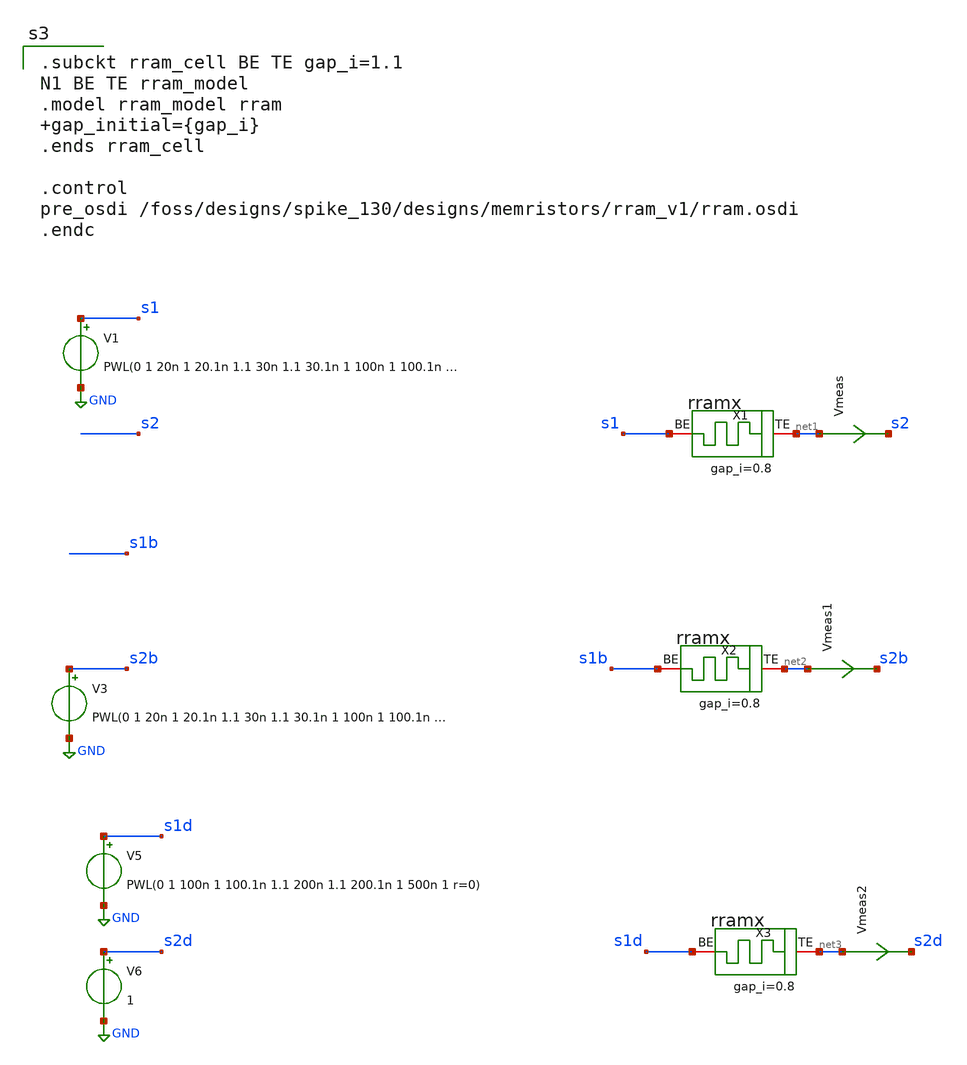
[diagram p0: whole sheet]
** sch_path: designs/tb_memristor/tb_stdp2.sch
**.subckt tb_stdp2
V1 s1 GND PWL(0 1 20n 1 20.1n 1.1 30n 1.1 30.1n 1 100n 1 100.1n 1.5 400n 1.5 400.1n 0.5 700n 0.5
+ 700.1n 1 1010n 1 1010.1n 1.1 1020n 1.1 1020.1n 1)
Vmeas net1 s2 0
.save i(vmeas)
X1 net1 s1 rram_cell gap_i=0.8
Vmeas1 net2 s2b 0
.save i(vmeas1)
X2 net2 s1b rram_cell gap_i=0.8
V5 s1d GND PWL(0 1 100n 1 100.1n 1.1 200n 1.1 200.1n 1 500n 1 r=0)
Vmeas2 net3 s2d 0
.save i(vmeas2)
X3 net3 s1d rram_cell gap_i=0.8
V6 s2d GND 1
V3 s2b GND PWL(0 1 20n 1 20.1n 1.1 30n 1.1 30.1n 1 100n 1 100.1n 1.5 400n 1.5 400.1n 0.5 700n 0.5
+ 700.1n 1 1010n 1 1010.1n 1.1 1020n 1.1 1020.1n 1)
**** begin user architecture code

.subckt rram_cell BE TE gap_i=1.1
N1 BE TE rram_model
.model rram_model rram gap_initial={gap_i}
.ends rram_cell

.control
pre_osdi /foss/designs/spike_130/designs/memristors/rram_v1/rram.osdi
.endc



*------------------ PARAMETROS BASE ------------------
.param t1=110n
.param t2=110.1n
.param t3=410n
.param t4=410.1n
.param t5=710n
.param t6=710.1n

*------------------ FUENTE PWL ------------------
V2 s2 0 PWL( 0 1  {t1} 1  {t2} 1.5  {t3} 1.5  {t4} 0.5  {t5} 0.5  {t6} 1)

V4 s1b 0 PWL( 0 1  {t1} 1  {t2} 1.5  {t3} 1.5  {t4} 0.5  {t5} 0.5  {t6} 1)

.tran 1n 1.1u

.control
  set wr_singlescale
  set wr_vecnames

  * variables internas del control
  let v1 = 110n
  let v2 = 110.1n
  let v3 = 410n
  let v4 = 410.1n
  let v5 = 700n
  let v6 = 700.1n

  let delta = 10n

  repeat 29

    alterparam t1 = $&v1
    alterparam t2 = $&v2
    alterparam t3 = $&v3
    alterparam t4 = $&v4
    alterparam t5 = $&v5
    alterparam t6 = $&v6

    reset
    run

    *remzerovec
    wrdata tb_stdp2.txt v(s1) v(s2) i(vmeas)
		+v(s1b) v(s2b) i(vmeas1)
    write tb_stdp2.raw
    set appendwrite

    * incrementar 10ns
    let v1 = v1 + delta
    let v2 = v2 + delta
    let v3 = v3 + delta
    let v4 = v4 + delta
    let v5 = v5 + delta
    let v6 = v6 + delta

  end

.endc
.save all
.end

**** end user architecture code
**.ends
.GLOBAL GND
.end
